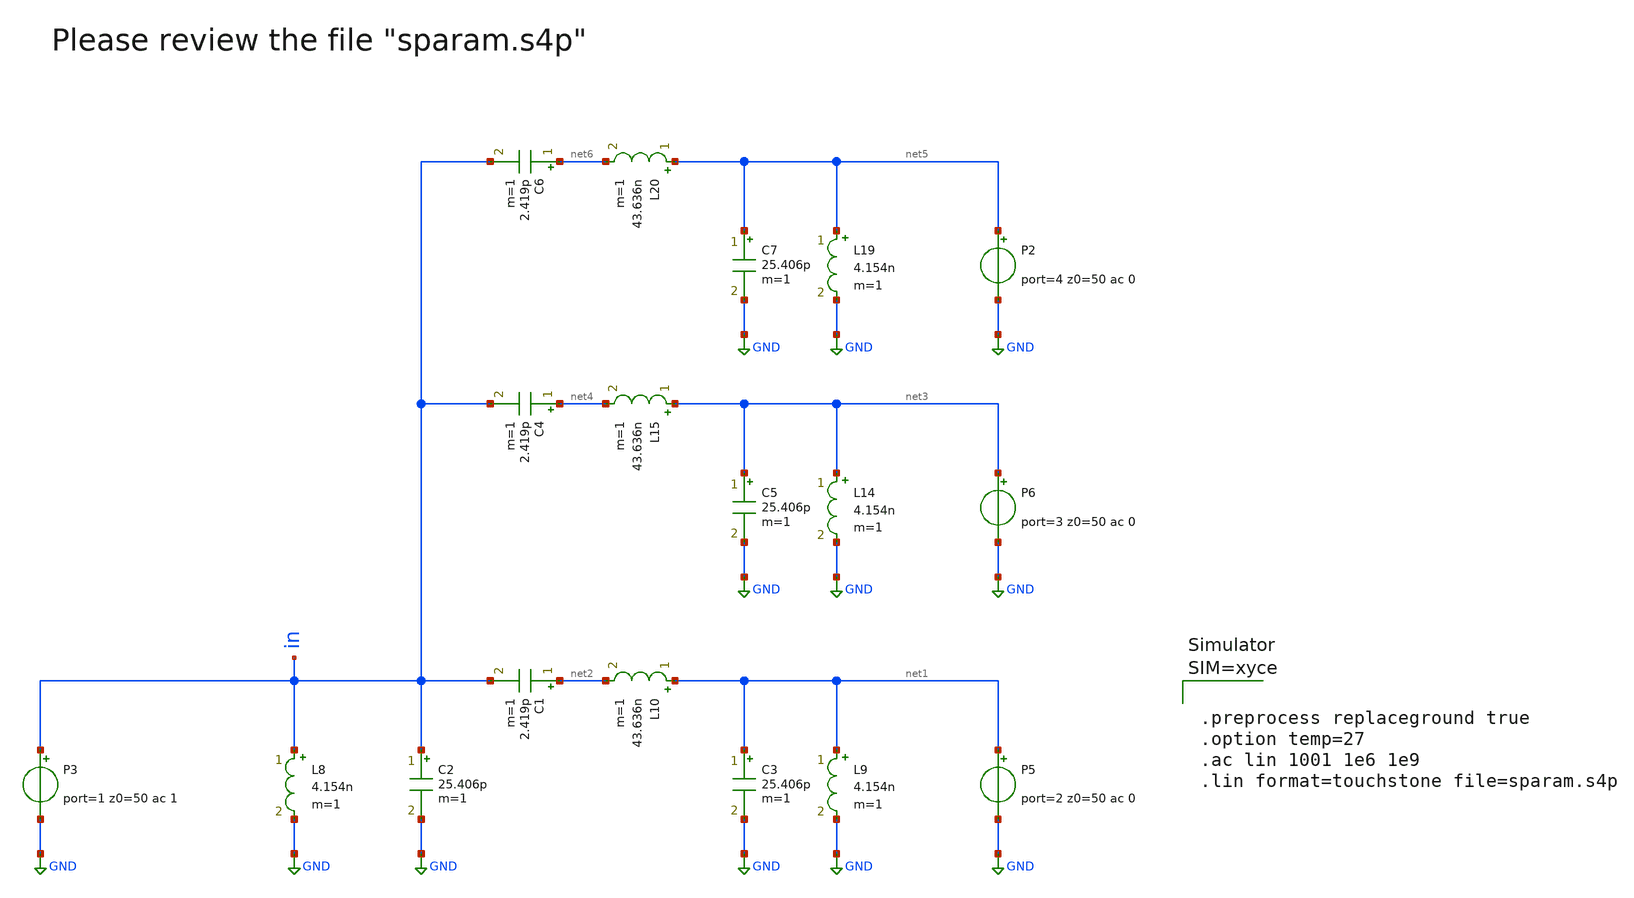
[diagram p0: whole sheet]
** sch_path: ihp-sg13g2/libs.tech/xschem/sg13g2_tests_xyce/sp_four_port.sch
* Copyright 2021 Stefan Frederik Schippers
* Licensed under the Apache License, Version 2.0 (the "License");
* you may not use this file except in compliance with the License.
* You may obtain a copy of the License at
* https://www.apache.org/licenses/LICENSE-2.0
* Unless required by applicable law or agreed to in writing, software
* distributed under the License is distributed on an "AS IS" BASIS,
* WITHOUT WARRANTIES OR CONDITIONS OF ANY KIND, either express or implied.
* See the License for the specific language governing permissions and
* limitations under the License.
* Copyright 2023 IHP PDK Authors
**.subckt sp_four_port
P3 in GND port=1 z0=50 ac 1
P5 net1 GND port=2 z0=50 ac 0
C1 net2 in 2.419p m=1
C2 in GND 25.406p m=1
C3 net1 GND 25.406p m=1
L8 in GND 4.154n m=1
L9 net1 GND 4.154n m=1
L10 net1 net2 43.636n m=1
P6 net3 GND port=3 z0=50 ac 0
C4 net4 in 2.419p m=1
C5 net3 GND 25.406p m=1
L14 net3 GND 4.154n m=1
L15 net3 net4 43.636n m=1
P2 net5 GND port=4 z0=50 ac 0
C6 net6 in 2.419p m=1
C7 net5 GND 25.406p m=1
L19 net5 GND 4.154n m=1
L20 net5 net6 43.636n m=1
**** begin user architecture code



**** end user architecture code
**.ends
.GLOBAL GND
.end
